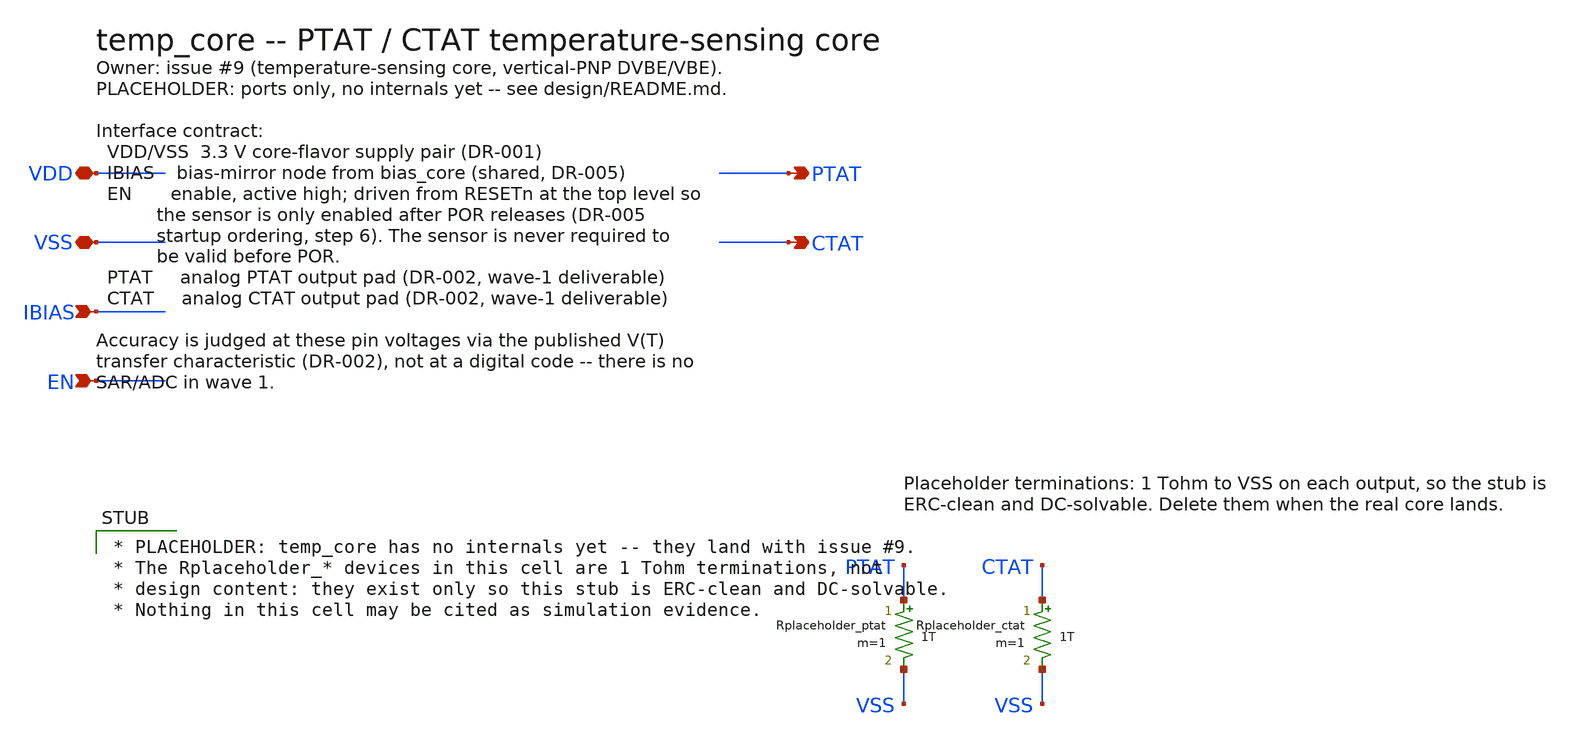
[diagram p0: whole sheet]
** sch_path: design/temp_core.sch
**.subckt temp_core VDD VSS IBIAS EN PTAT CTAT
*.iopin VDD
*.iopin VSS
*.ipin IBIAS
*.ipin EN
*.opin PTAT
*.opin CTAT
Rplaceholder_ptat PTAT VSS 1T m=1
Rplaceholder_ctat CTAT VSS 1T m=1
**** begin user architecture code

* PLACEHOLDER: temp_core has no internals yet -- they land with issue #9.
* The Rplaceholder_* devices in this cell are 1 Tohm terminations, not
* design content: they exist only so this stub is ERC-clean and DC-solvable.
* Nothing in this cell may be cited as simulation evidence.

**** end user architecture code
**.ends
.end
